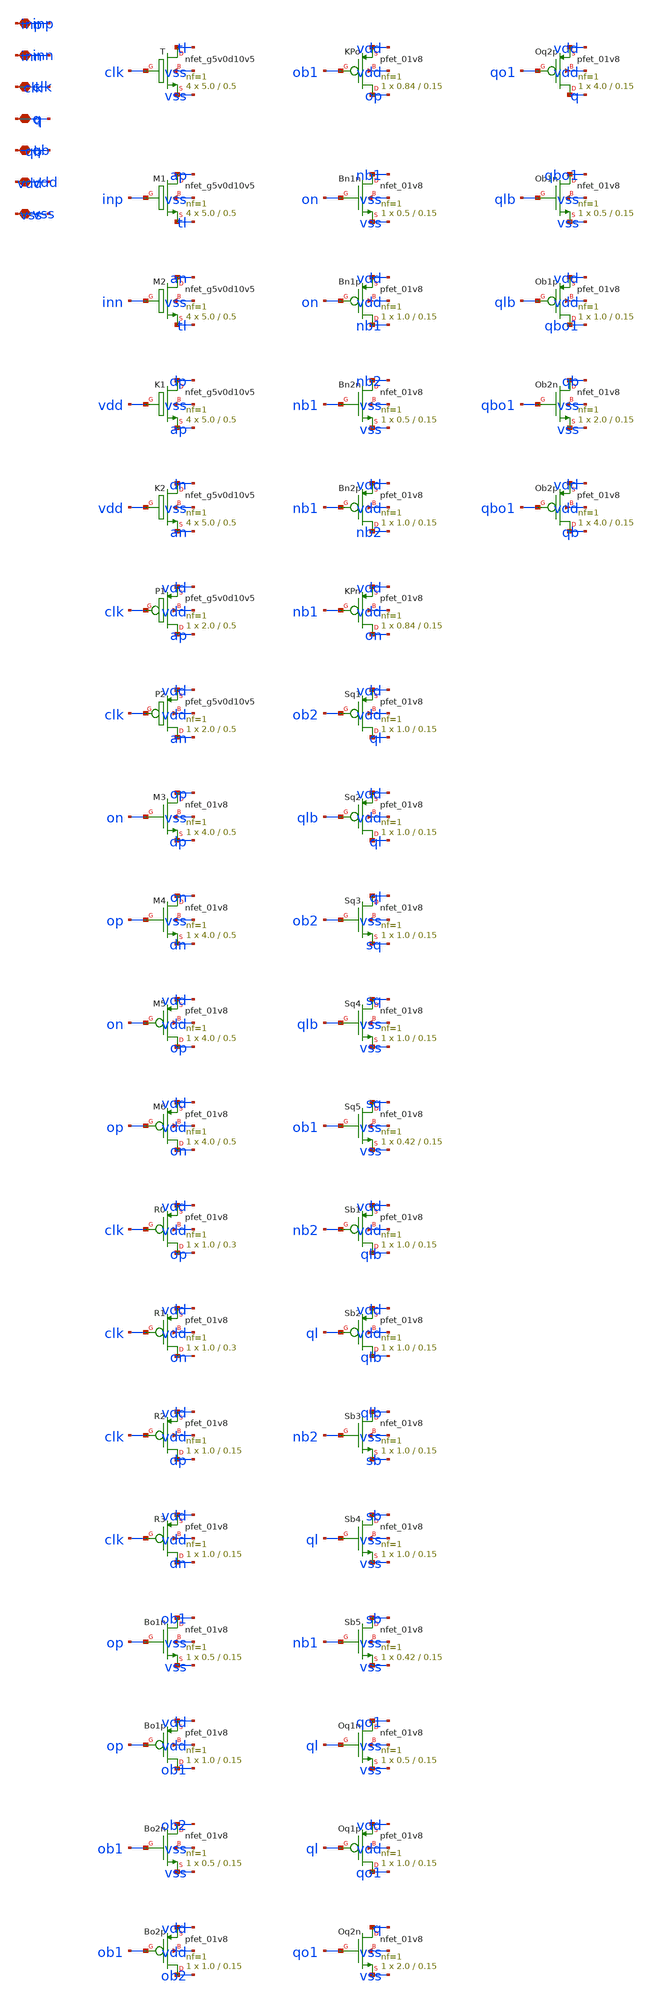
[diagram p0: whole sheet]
** sch_path: design/xschem/sch/c3_comp.sch
**.subckt c3_comp inp inn clk q qb vdd vss
*.iopin inp
*.iopin inn
*.iopin clk
*.iopin q
*.iopin qb
*.iopin vdd
*.iopin vss
XT tl clk vss vss sky130_fd_pr__nfet_g5v0d10v5 L=0.5 W=5.0 nf=1 ad='int((1 + 1)/2) * 5.0 / 1 * 0.29'
+ as='int((1 + 2)/2) * 5.0 / 1 * 0.29' pd='2*int((1 + 1)/2) * (5.0 / 1 + 0.29)' ps='2*int((1 + 2)/2) * (5.0 / 1 + 0.29)'
+ nrd='0.29 / 5.0 ' nrs='0.29 / 5.0 ' sa=0 sb=0 sd=0 mult=4 m=4
XM1 ap inp tl vss sky130_fd_pr__nfet_g5v0d10v5 L=0.5 W=5.0 nf=1 ad='int((1 + 1)/2) * 5.0 / 1 * 0.29'
+ as='int((1 + 2)/2) * 5.0 / 1 * 0.29' pd='2*int((1 + 1)/2) * (5.0 / 1 + 0.29)' ps='2*int((1 + 2)/2) * (5.0 / 1 + 0.29)'
+ nrd='0.29 / 5.0 ' nrs='0.29 / 5.0 ' sa=0 sb=0 sd=0 mult=4 m=4
XM2 an inn tl vss sky130_fd_pr__nfet_g5v0d10v5 L=0.5 W=5.0 nf=1 ad='int((1 + 1)/2) * 5.0 / 1 * 0.29'
+ as='int((1 + 2)/2) * 5.0 / 1 * 0.29' pd='2*int((1 + 1)/2) * (5.0 / 1 + 0.29)' ps='2*int((1 + 2)/2) * (5.0 / 1 + 0.29)'
+ nrd='0.29 / 5.0 ' nrs='0.29 / 5.0 ' sa=0 sb=0 sd=0 mult=4 m=4
XK1 dp vdd ap vss sky130_fd_pr__nfet_g5v0d10v5 L=0.5 W=5.0 nf=1 ad='int((1 + 1)/2) * 5.0 / 1 * 0.29'
+ as='int((1 + 2)/2) * 5.0 / 1 * 0.29' pd='2*int((1 + 1)/2) * (5.0 / 1 + 0.29)' ps='2*int((1 + 2)/2) * (5.0 / 1 + 0.29)'
+ nrd='0.29 / 5.0 ' nrs='0.29 / 5.0 ' sa=0 sb=0 sd=0 mult=4 m=4
XK2 dn vdd an vss sky130_fd_pr__nfet_g5v0d10v5 L=0.5 W=5.0 nf=1 ad='int((1 + 1)/2) * 5.0 / 1 * 0.29'
+ as='int((1 + 2)/2) * 5.0 / 1 * 0.29' pd='2*int((1 + 1)/2) * (5.0 / 1 + 0.29)' ps='2*int((1 + 2)/2) * (5.0 / 1 + 0.29)'
+ nrd='0.29 / 5.0 ' nrs='0.29 / 5.0 ' sa=0 sb=0 sd=0 mult=4 m=4
XP1 ap clk vdd vdd sky130_fd_pr__pfet_g5v0d10v5 L=0.5 W=2.0 nf=1 ad='int((1 + 1)/2) * 2.0 / 1 * 0.29'
+ as='int((1 + 2)/2) * 2.0 / 1 * 0.29' pd='2*int((1 + 1)/2) * (2.0 / 1 + 0.29)' ps='2*int((1 + 2)/2) * (2.0 / 1 + 0.29)'
+ nrd='0.29 / 2.0 ' nrs='0.29 / 2.0 ' sa=0 sb=0 sd=0 mult=1 m=1
XP2 an clk vdd vdd sky130_fd_pr__pfet_g5v0d10v5 L=0.5 W=2.0 nf=1 ad='int((1 + 1)/2) * 2.0 / 1 * 0.29'
+ as='int((1 + 2)/2) * 2.0 / 1 * 0.29' pd='2*int((1 + 1)/2) * (2.0 / 1 + 0.29)' ps='2*int((1 + 2)/2) * (2.0 / 1 + 0.29)'
+ nrd='0.29 / 2.0 ' nrs='0.29 / 2.0 ' sa=0 sb=0 sd=0 mult=1 m=1
XM3 op on dp vss sky130_fd_pr__nfet_01v8 L=0.5 W=4.0 nf=1 ad='int((1 + 1)/2) * 4.0 / 1 * 0.29' as='int((1 + 2)/2) * 4.0 / 1 * 0.29'
+ pd='2*int((1 + 1)/2) * (4.0 / 1 + 0.29)' ps='2*int((1 + 2)/2) * (4.0 / 1 + 0.29)' nrd='0.29 / 4.0 ' nrs='0.29 / 4.0 '
+ sa=0 sb=0 sd=0 mult=1 m=1
XM4 on op dn vss sky130_fd_pr__nfet_01v8 L=0.5 W=4.0 nf=1 ad='int((1 + 1)/2) * 4.0 / 1 * 0.29' as='int((1 + 2)/2) * 4.0 / 1 * 0.29'
+ pd='2*int((1 + 1)/2) * (4.0 / 1 + 0.29)' ps='2*int((1 + 2)/2) * (4.0 / 1 + 0.29)' nrd='0.29 / 4.0 ' nrs='0.29 / 4.0 '
+ sa=0 sb=0 sd=0 mult=1 m=1
XM5 op on vdd vdd sky130_fd_pr__pfet_01v8 L=0.5 W=4.0 nf=1 ad='int((nf+1)/2) * W/nf * 0.29' as='int((nf+2)/2) * W/nf * 0.29'
+ pd='2*int((nf+1)/2) * (W/nf + 0.29)' ps='2*int((nf+2)/2) * (W/nf + 0.29)' nrd='0.29 / W' nrs='0.29 / W'
+ sa=0 sb=0 sd=0 mult=1 m=1
XM6 on op vdd vdd sky130_fd_pr__pfet_01v8 L=0.5 W=4.0 nf=1 ad='int((nf+1)/2) * W/nf * 0.29' as='int((nf+2)/2) * W/nf * 0.29'
+ pd='2*int((nf+1)/2) * (W/nf + 0.29)' ps='2*int((nf+2)/2) * (W/nf + 0.29)' nrd='0.29 / W' nrs='0.29 / W'
+ sa=0 sb=0 sd=0 mult=1 m=1
XR0 op clk vdd vdd sky130_fd_pr__pfet_01v8 L=0.3 W=1.0 nf=1 ad='int((nf+1)/2) * W/nf * 0.29' as='int((nf+2)/2) * W/nf * 0.29'
+ pd='2*int((nf+1)/2) * (W/nf + 0.29)' ps='2*int((nf+2)/2) * (W/nf + 0.29)' nrd='0.29 / W' nrs='0.29 / W'
+ sa=0 sb=0 sd=0 mult=1 m=1
XR1 on clk vdd vdd sky130_fd_pr__pfet_01v8 L=0.3 W=1.0 nf=1 ad='int((nf+1)/2) * W/nf * 0.29' as='int((nf+2)/2) * W/nf * 0.29'
+ pd='2*int((nf+1)/2) * (W/nf + 0.29)' ps='2*int((nf+2)/2) * (W/nf + 0.29)' nrd='0.29 / W' nrs='0.29 / W'
+ sa=0 sb=0 sd=0 mult=1 m=1
XR2 dp clk vdd vdd sky130_fd_pr__pfet_01v8 L=0.15 W=1.0 nf=1 ad='int((nf+1)/2) * W/nf * 0.29' as='int((nf+2)/2) * W/nf * 0.29'
+ pd='2*int((nf+1)/2) * (W/nf + 0.29)' ps='2*int((nf+2)/2) * (W/nf + 0.29)' nrd='0.29 / W' nrs='0.29 / W'
+ sa=0 sb=0 sd=0 mult=1 m=1
XR3 dn clk vdd vdd sky130_fd_pr__pfet_01v8 L=0.15 W=1.0 nf=1 ad='int((nf+1)/2) * W/nf * 0.29' as='int((nf+2)/2) * W/nf * 0.29'
+ pd='2*int((nf+1)/2) * (W/nf + 0.29)' ps='2*int((nf+2)/2) * (W/nf + 0.29)' nrd='0.29 / W' nrs='0.29 / W'
+ sa=0 sb=0 sd=0 mult=1 m=1
XBo1n ob1 op vss vss sky130_fd_pr__nfet_01v8 L=0.15 W=0.5 nf=1 ad='int((1 + 1)/2) * 0.5 / 1 * 0.29' as='int((1 + 2)/2) * 0.5 / 1 * 0.29'
+ pd='2*int((1 + 1)/2) * (0.5 / 1 + 0.29)' ps='2*int((1 + 2)/2) * (0.5 / 1 + 0.29)' nrd='0.29 / 0.5 ' nrs='0.29 / 0.5 '
+ sa=0 sb=0 sd=0 mult=1 m=1
XBo1p ob1 op vdd vdd sky130_fd_pr__pfet_01v8 L=0.15 W=1.0 nf=1 ad='int((nf+1)/2) * W/nf * 0.29' as='int((nf+2)/2) * W/nf * 0.29'
+ pd='2*int((nf+1)/2) * (W/nf + 0.29)' ps='2*int((nf+2)/2) * (W/nf + 0.29)' nrd='0.29 / W' nrs='0.29 / W'
+ sa=0 sb=0 sd=0 mult=1 m=1
XBo2n ob2 ob1 vss vss sky130_fd_pr__nfet_01v8 L=0.15 W=0.5 nf=1 ad='int((1 + 1)/2) * 0.5 / 1 * 0.29'
+ as='int((1 + 2)/2) * 0.5 / 1 * 0.29' pd='2*int((1 + 1)/2) * (0.5 / 1 + 0.29)' ps='2*int((1 + 2)/2) * (0.5 / 1 + 0.29)'
+ nrd='0.29 / 0.5 ' nrs='0.29 / 0.5 ' sa=0 sb=0 sd=0 mult=1 m=1
XBo2p ob2 ob1 vdd vdd sky130_fd_pr__pfet_01v8 L=0.15 W=1.0 nf=1 ad='int((nf+1)/2) * W/nf * 0.29' as='int((nf+2)/2) * W/nf * 0.29'
+ pd='2*int((nf+1)/2) * (W/nf + 0.29)' ps='2*int((nf+2)/2) * (W/nf + 0.29)' nrd='0.29 / W' nrs='0.29 / W'
+ sa=0 sb=0 sd=0 mult=1 m=1
XKPo op ob1 vdd vdd sky130_fd_pr__pfet_01v8 L=0.15 W=0.84 nf=1 ad='int((nf+1)/2) * W/nf * 0.29' as='int((nf+2)/2) * W/nf * 0.29'
+ pd='2*int((nf+1)/2) * (W/nf + 0.29)' ps='2*int((nf+2)/2) * (W/nf + 0.29)' nrd='0.29 / W' nrs='0.29 / W'
+ sa=0 sb=0 sd=0 mult=1 m=1
XBn1n nb1 on vss vss sky130_fd_pr__nfet_01v8 L=0.15 W=0.5 nf=1 ad='int((1 + 1)/2) * 0.5 / 1 * 0.29' as='int((1 + 2)/2) * 0.5 / 1 * 0.29'
+ pd='2*int((1 + 1)/2) * (0.5 / 1 + 0.29)' ps='2*int((1 + 2)/2) * (0.5 / 1 + 0.29)' nrd='0.29 / 0.5 ' nrs='0.29 / 0.5 '
+ sa=0 sb=0 sd=0 mult=1 m=1
XBn1p nb1 on vdd vdd sky130_fd_pr__pfet_01v8 L=0.15 W=1.0 nf=1 ad='int((nf+1)/2) * W/nf * 0.29' as='int((nf+2)/2) * W/nf * 0.29'
+ pd='2*int((nf+1)/2) * (W/nf + 0.29)' ps='2*int((nf+2)/2) * (W/nf + 0.29)' nrd='0.29 / W' nrs='0.29 / W'
+ sa=0 sb=0 sd=0 mult=1 m=1
XBn2n nb2 nb1 vss vss sky130_fd_pr__nfet_01v8 L=0.15 W=0.5 nf=1 ad='int((1 + 1)/2) * 0.5 / 1 * 0.29'
+ as='int((1 + 2)/2) * 0.5 / 1 * 0.29' pd='2*int((1 + 1)/2) * (0.5 / 1 + 0.29)' ps='2*int((1 + 2)/2) * (0.5 / 1 + 0.29)'
+ nrd='0.29 / 0.5 ' nrs='0.29 / 0.5 ' sa=0 sb=0 sd=0 mult=1 m=1
XBn2p nb2 nb1 vdd vdd sky130_fd_pr__pfet_01v8 L=0.15 W=1.0 nf=1 ad='int((nf+1)/2) * W/nf * 0.29' as='int((nf+2)/2) * W/nf * 0.29'
+ pd='2*int((nf+1)/2) * (W/nf + 0.29)' ps='2*int((nf+2)/2) * (W/nf + 0.29)' nrd='0.29 / W' nrs='0.29 / W'
+ sa=0 sb=0 sd=0 mult=1 m=1
XKPn on nb1 vdd vdd sky130_fd_pr__pfet_01v8 L=0.15 W=0.84 nf=1 ad='int((nf+1)/2) * W/nf * 0.29' as='int((nf+2)/2) * W/nf * 0.29'
+ pd='2*int((nf+1)/2) * (W/nf + 0.29)' ps='2*int((nf+2)/2) * (W/nf + 0.29)' nrd='0.29 / W' nrs='0.29 / W'
+ sa=0 sb=0 sd=0 mult=1 m=1
XSq1 ql ob2 vdd vdd sky130_fd_pr__pfet_01v8 L=0.15 W=1.0 nf=1 ad='int((nf+1)/2) * W/nf * 0.29' as='int((nf+2)/2) * W/nf * 0.29'
+ pd='2*int((nf+1)/2) * (W/nf + 0.29)' ps='2*int((nf+2)/2) * (W/nf + 0.29)' nrd='0.29 / W' nrs='0.29 / W'
+ sa=0 sb=0 sd=0 mult=1 m=1
XSq2 ql qlb vdd vdd sky130_fd_pr__pfet_01v8 L=0.15 W=1.0 nf=1 ad='int((nf+1)/2) * W/nf * 0.29' as='int((nf+2)/2) * W/nf * 0.29'
+ pd='2*int((nf+1)/2) * (W/nf + 0.29)' ps='2*int((nf+2)/2) * (W/nf + 0.29)' nrd='0.29 / W' nrs='0.29 / W'
+ sa=0 sb=0 sd=0 mult=1 m=1
XSq3 ql ob2 sq vss sky130_fd_pr__nfet_01v8 L=0.15 W=1.0 nf=1 ad='int((1 + 1)/2) * 1.0 / 1 * 0.29' as='int((1 + 2)/2) * 1.0 / 1 * 0.29'
+ pd='2*int((1 + 1)/2) * (1.0 / 1 + 0.29)' ps='2*int((1 + 2)/2) * (1.0 / 1 + 0.29)' nrd='0.29 / 1.0 ' nrs='0.29 / 1.0 '
+ sa=0 sb=0 sd=0 mult=1 m=1
XSq4 sq qlb vss vss sky130_fd_pr__nfet_01v8 L=0.15 W=1.0 nf=1 ad='int((1 + 1)/2) * 1.0 / 1 * 0.29' as='int((1 + 2)/2) * 1.0 / 1 * 0.29'
+ pd='2*int((1 + 1)/2) * (1.0 / 1 + 0.29)' ps='2*int((1 + 2)/2) * (1.0 / 1 + 0.29)' nrd='0.29 / 1.0 ' nrs='0.29 / 1.0 '
+ sa=0 sb=0 sd=0 mult=1 m=1
XSq5 sq ob1 vss vss sky130_fd_pr__nfet_01v8 L=0.15 W=0.42 nf=1 ad='int((1 + 1)/2) * 0.42 / 1 * 0.29'
+ as='int((1 + 2)/2) * 0.42 / 1 * 0.29' pd='2*int((1 + 1)/2) * (0.42 / 1 + 0.29)' ps='2*int((1 + 2)/2) * (0.42 / 1 + 0.29)'
+ nrd='0.29 / 0.42 ' nrs='0.29 / 0.42 ' sa=0 sb=0 sd=0 mult=1 m=1
XSb1 qlb nb2 vdd vdd sky130_fd_pr__pfet_01v8 L=0.15 W=1.0 nf=1 ad='int((nf+1)/2) * W/nf * 0.29' as='int((nf+2)/2) * W/nf * 0.29'
+ pd='2*int((nf+1)/2) * (W/nf + 0.29)' ps='2*int((nf+2)/2) * (W/nf + 0.29)' nrd='0.29 / W' nrs='0.29 / W'
+ sa=0 sb=0 sd=0 mult=1 m=1
XSb2 qlb ql vdd vdd sky130_fd_pr__pfet_01v8 L=0.15 W=1.0 nf=1 ad='int((nf+1)/2) * W/nf * 0.29' as='int((nf+2)/2) * W/nf * 0.29'
+ pd='2*int((nf+1)/2) * (W/nf + 0.29)' ps='2*int((nf+2)/2) * (W/nf + 0.29)' nrd='0.29 / W' nrs='0.29 / W'
+ sa=0 sb=0 sd=0 mult=1 m=1
XSb3 qlb nb2 sb vss sky130_fd_pr__nfet_01v8 L=0.15 W=1.0 nf=1 ad='int((1 + 1)/2) * 1.0 / 1 * 0.29' as='int((1 + 2)/2) * 1.0 / 1 * 0.29'
+ pd='2*int((1 + 1)/2) * (1.0 / 1 + 0.29)' ps='2*int((1 + 2)/2) * (1.0 / 1 + 0.29)' nrd='0.29 / 1.0 ' nrs='0.29 / 1.0 '
+ sa=0 sb=0 sd=0 mult=1 m=1
XSb4 sb ql vss vss sky130_fd_pr__nfet_01v8 L=0.15 W=1.0 nf=1 ad='int((1 + 1)/2) * 1.0 / 1 * 0.29' as='int((1 + 2)/2) * 1.0 / 1 * 0.29'
+ pd='2*int((1 + 1)/2) * (1.0 / 1 + 0.29)' ps='2*int((1 + 2)/2) * (1.0 / 1 + 0.29)' nrd='0.29 / 1.0 ' nrs='0.29 / 1.0 '
+ sa=0 sb=0 sd=0 mult=1 m=1
XSb5 sb nb1 vss vss sky130_fd_pr__nfet_01v8 L=0.15 W=0.42 nf=1 ad='int((1 + 1)/2) * 0.42 / 1 * 0.29'
+ as='int((1 + 2)/2) * 0.42 / 1 * 0.29' pd='2*int((1 + 1)/2) * (0.42 / 1 + 0.29)' ps='2*int((1 + 2)/2) * (0.42 / 1 + 0.29)'
+ nrd='0.29 / 0.42 ' nrs='0.29 / 0.42 ' sa=0 sb=0 sd=0 mult=1 m=1
XOq1n qo1 ql vss vss sky130_fd_pr__nfet_01v8 L=0.15 W=0.5 nf=1 ad='int((1 + 1)/2) * 0.5 / 1 * 0.29' as='int((1 + 2)/2) * 0.5 / 1 * 0.29'
+ pd='2*int((1 + 1)/2) * (0.5 / 1 + 0.29)' ps='2*int((1 + 2)/2) * (0.5 / 1 + 0.29)' nrd='0.29 / 0.5 ' nrs='0.29 / 0.5 '
+ sa=0 sb=0 sd=0 mult=1 m=1
XOq1p qo1 ql vdd vdd sky130_fd_pr__pfet_01v8 L=0.15 W=1.0 nf=1 ad='int((nf+1)/2) * W/nf * 0.29' as='int((nf+2)/2) * W/nf * 0.29'
+ pd='2*int((nf+1)/2) * (W/nf + 0.29)' ps='2*int((nf+2)/2) * (W/nf + 0.29)' nrd='0.29 / W' nrs='0.29 / W'
+ sa=0 sb=0 sd=0 mult=1 m=1
XOq2n q qo1 vss vss sky130_fd_pr__nfet_01v8 L=0.15 W=2.0 nf=1 ad='int((1 + 1)/2) * 2.0 / 1 * 0.29' as='int((1 + 2)/2) * 2.0 / 1 * 0.29'
+ pd='2*int((1 + 1)/2) * (2.0 / 1 + 0.29)' ps='2*int((1 + 2)/2) * (2.0 / 1 + 0.29)' nrd='0.29 / 2.0 ' nrs='0.29 / 2.0 '
+ sa=0 sb=0 sd=0 mult=1 m=1
XOq2p q qo1 vdd vdd sky130_fd_pr__pfet_01v8 L=0.15 W=4.0 nf=1 ad='int((nf+1)/2) * W/nf * 0.29' as='int((nf+2)/2) * W/nf * 0.29'
+ pd='2*int((nf+1)/2) * (W/nf + 0.29)' ps='2*int((nf+2)/2) * (W/nf + 0.29)' nrd='0.29 / W' nrs='0.29 / W'
+ sa=0 sb=0 sd=0 mult=1 m=1
XOb1n qbo1 qlb vss vss sky130_fd_pr__nfet_01v8 L=0.15 W=0.5 nf=1 ad='int((1 + 1)/2) * 0.5 / 1 * 0.29'
+ as='int((1 + 2)/2) * 0.5 / 1 * 0.29' pd='2*int((1 + 1)/2) * (0.5 / 1 + 0.29)' ps='2*int((1 + 2)/2) * (0.5 / 1 + 0.29)'
+ nrd='0.29 / 0.5 ' nrs='0.29 / 0.5 ' sa=0 sb=0 sd=0 mult=1 m=1
XOb1p qbo1 qlb vdd vdd sky130_fd_pr__pfet_01v8 L=0.15 W=1.0 nf=1 ad='int((nf+1)/2) * W/nf * 0.29' as='int((nf+2)/2) * W/nf * 0.29'
+ pd='2*int((nf+1)/2) * (W/nf + 0.29)' ps='2*int((nf+2)/2) * (W/nf + 0.29)' nrd='0.29 / W' nrs='0.29 / W'
+ sa=0 sb=0 sd=0 mult=1 m=1
XOb2n qb qbo1 vss vss sky130_fd_pr__nfet_01v8 L=0.15 W=2.0 nf=1 ad='int((1 + 1)/2) * 2.0 / 1 * 0.29'
+ as='int((1 + 2)/2) * 2.0 / 1 * 0.29' pd='2*int((1 + 1)/2) * (2.0 / 1 + 0.29)' ps='2*int((1 + 2)/2) * (2.0 / 1 + 0.29)'
+ nrd='0.29 / 2.0 ' nrs='0.29 / 2.0 ' sa=0 sb=0 sd=0 mult=1 m=1
XOb2p qb qbo1 vdd vdd sky130_fd_pr__pfet_01v8 L=0.15 W=4.0 nf=1 ad='int((nf+1)/2) * W/nf * 0.29' as='int((nf+2)/2) * W/nf * 0.29'
+ pd='2*int((nf+1)/2) * (W/nf + 0.29)' ps='2*int((nf+2)/2) * (W/nf + 0.29)' nrd='0.29 / W' nrs='0.29 / W'
+ sa=0 sb=0 sd=0 mult=1 m=1
**.ends
.end
